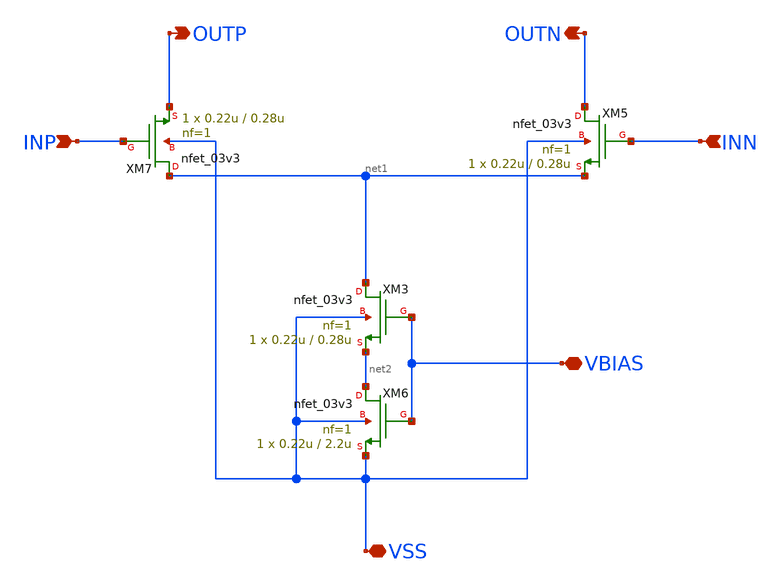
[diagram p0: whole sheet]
** sch_path: xschem/CS_Switch_1x1.sch
**.subckt CS_Switch_1x1 INP INN OUTP OUTN VBIAS VSS
*.ipin INP
*.ipin INN
*.opin OUTP
*.opin OUTN
*.iopin VBIAS
*.iopin VSS
XM3 net1 VBIAS net2 VSS nfet_03v3 L=0.28u W=0.22u nf=1 ad='int((nf+1)/2) * W/nf * 0.18u' as='int((nf+2)/2) * W/nf * 0.18u'
+ pd='2*int((nf+1)/2) * (W/nf + 0.18u)' ps='2*int((nf+2)/2) * (W/nf + 0.18u)' nrd='0.18u / W' nrs='0.18u / W'
+ sa=0 sb=0 sd=0 m=1
XM6 net2 VBIAS VSS VSS nfet_03v3 L=2.2u W=0.22u nf=1 ad='int((nf+1)/2) * W/nf * 0.18u' as='int((nf+2)/2) * W/nf * 0.18u'
+ pd='2*int((nf+1)/2) * (W/nf + 0.18u)' ps='2*int((nf+2)/2) * (W/nf + 0.18u)' nrd='0.18u / W' nrs='0.18u / W'
+ sa=0 sb=0 sd=0 m=1
XM5 OUTN INN net1 VSS nfet_03v3 L=0.28u W=0.22u nf=1 ad='int((nf+1)/2) * W/nf * 0.18u' as='int((nf+2)/2) * W/nf * 0.18u'
+ pd='2*int((nf+1)/2) * (W/nf + 0.18u)' ps='2*int((nf+2)/2) * (W/nf + 0.18u)' nrd='0.18u / W' nrs='0.18u / W'
+ sa=0 sb=0 sd=0 m=1
XM7 net1 INP OUTP VSS nfet_03v3 L=0.28u W=0.22u nf=1 ad='int((nf+1)/2) * W/nf * 0.18u' as='int((nf+2)/2) * W/nf * 0.18u'
+ pd='2*int((nf+1)/2) * (W/nf + 0.18u)' ps='2*int((nf+2)/2) * (W/nf + 0.18u)' nrd='0.18u / W' nrs='0.18u / W'
+ sa=0 sb=0 sd=0 m=1
**.ends
.end
